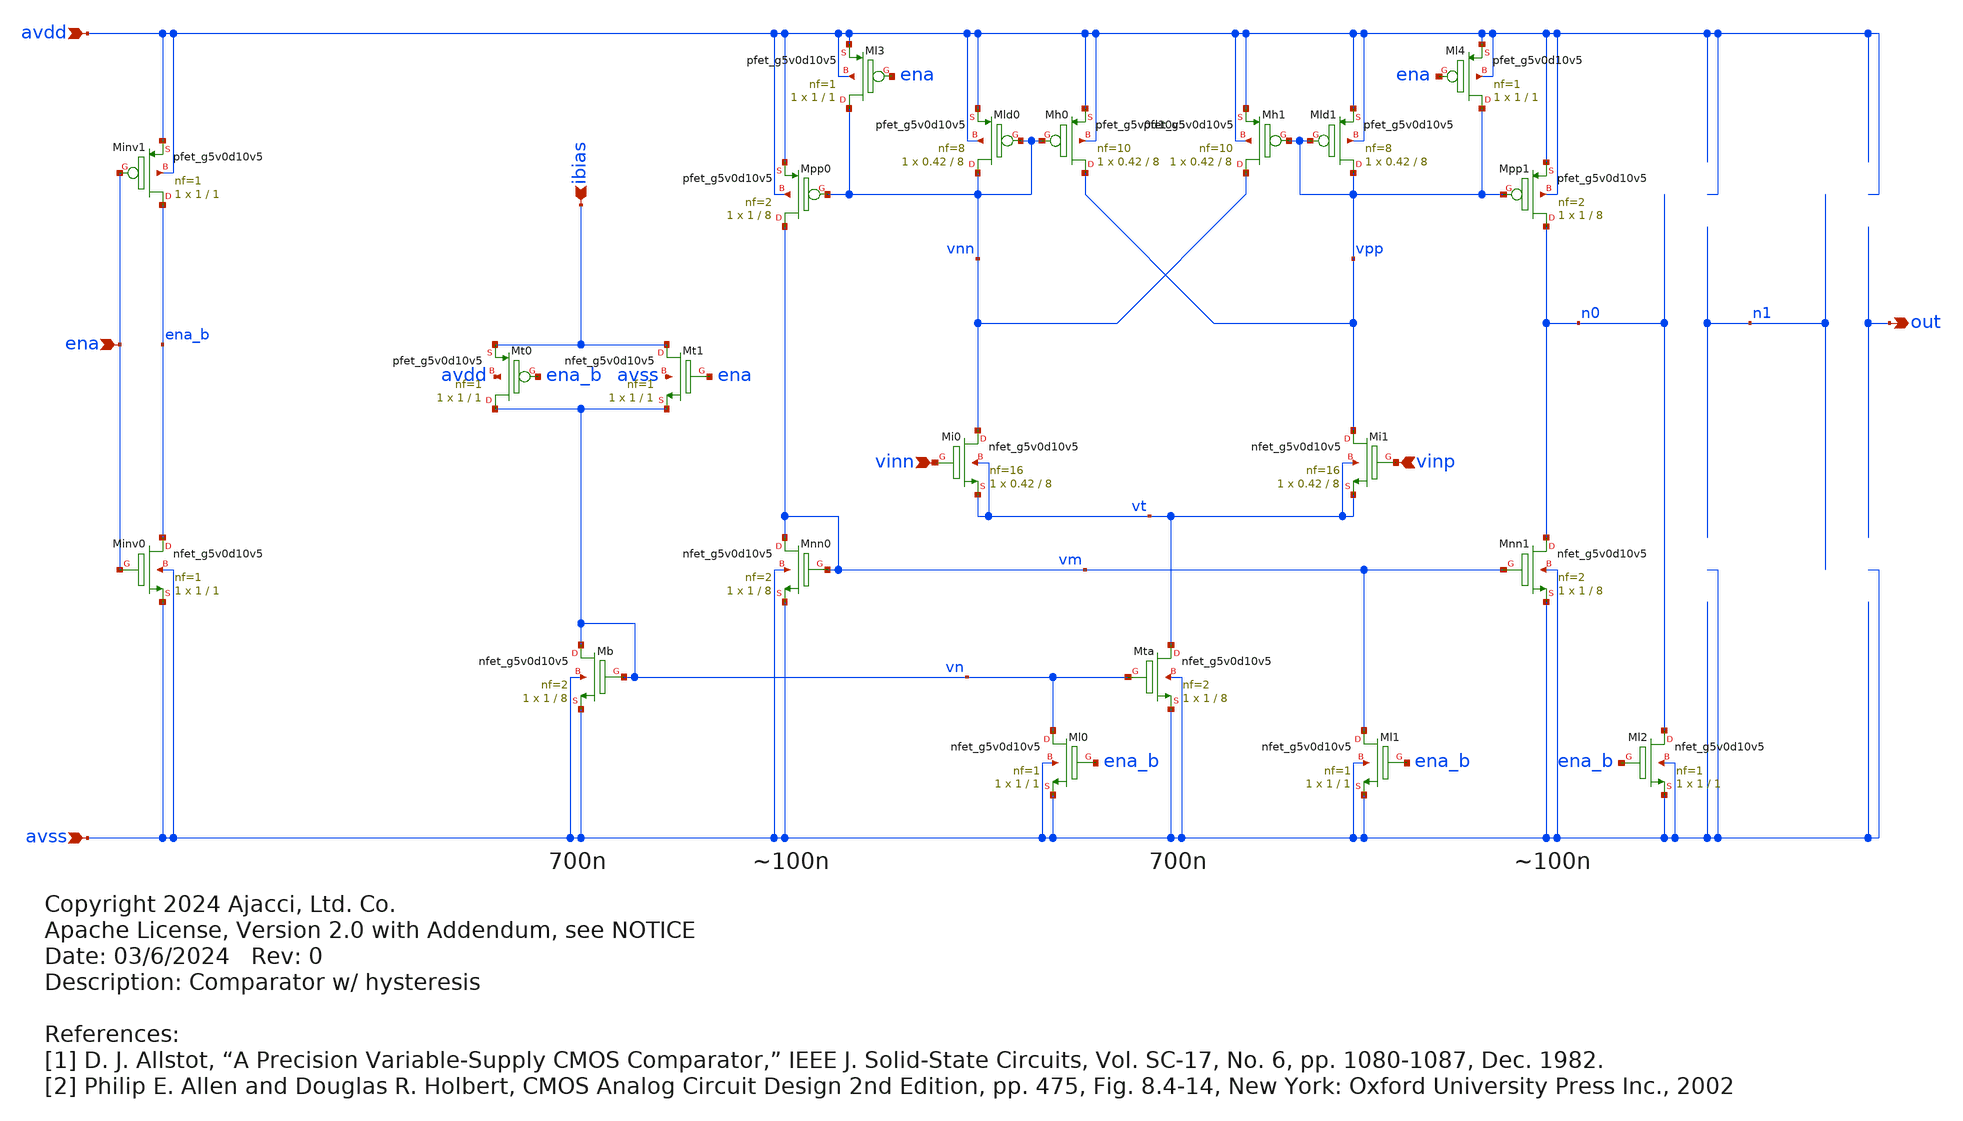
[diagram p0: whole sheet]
** sch_path: xschem/comparator_wip.sch
* Copyright 2024 Ajacci, Ltd. Co.
* Apache License, Version 2.0 with Addendum, see NOTICE
**.subckt comparator_wip ena avdd avss ibias vinn vinp out
*.ipin ena
*.ipin avdd
*.ipin avss
*.ipin ibias
*.ipin vinn
*.ipin vinp
*.opin out
XMi0 vnn vinn vt vt sky130_fd_pr__nfet_g5v0d10v5 L=8 W=0.42 nf=16 ad='int((nf+1)/2) * W/nf * 0.29' as='int((nf+2)/2) * W/nf * 0.29'
+ pd='2*int((nf+1)/2) * (W/nf + 0.29)' ps='2*int((nf+2)/2) * (W/nf + 0.29)' nrd='0.29 / W' nrs='0.29 / W'
+ sa=0 sb=0 sd=0 mult=1 m=1
XMi1 vpp vinp vt vt sky130_fd_pr__nfet_g5v0d10v5 L=8 W=0.42 nf=16 ad='int((nf+1)/2) * W/nf * 0.29' as='int((nf+2)/2) * W/nf * 0.29'
+ pd='2*int((nf+1)/2) * (W/nf + 0.29)' ps='2*int((nf+2)/2) * (W/nf + 0.29)' nrd='0.29 / W' nrs='0.29 / W'
+ sa=0 sb=0 sd=0 mult=1 m=1
XMb vn vn avss avss sky130_fd_pr__nfet_g5v0d10v5 L=8 W=1 nf=2 ad='int((nf+1)/2) * W/nf * 0.29' as='int((nf+2)/2) * W/nf * 0.29'
+ pd='2*int((nf+1)/2) * (W/nf + 0.29)' ps='2*int((nf+2)/2) * (W/nf + 0.29)' nrd='0.29 / W' nrs='0.29 / W'
+ sa=0 sb=0 sd=0 mult=1 m=1
XMta vt vn avss avss sky130_fd_pr__nfet_g5v0d10v5 L=8 W=1 nf=2 ad='int((nf+1)/2) * W/nf * 0.29' as='int((nf+2)/2) * W/nf * 0.29'
+ pd='2*int((nf+1)/2) * (W/nf + 0.29)' ps='2*int((nf+2)/2) * (W/nf + 0.29)' nrd='0.29 / W' nrs='0.29 / W'
+ sa=0 sb=0 sd=0 mult=1 m=1
XMld1 vpp vpp avdd avdd sky130_fd_pr__pfet_g5v0d10v5 L=8 W=0.42 nf=8 ad='int((nf+1)/2) * W/nf * 0.29'
+ as='int((nf+2)/2) * W/nf * 0.29' pd='2*int((nf+1)/2) * (W/nf + 0.29)' ps='2*int((nf+2)/2) * (W/nf + 0.29)'
+ nrd='0.29 / W' nrs='0.29 / W' sa=0 sb=0 sd=0 mult=1 m=1
XMh1 vnn vpp avdd avdd sky130_fd_pr__pfet_g5v0d10v5 L=8 W=0.42 nf=10 ad='int((nf+1)/2) * W/nf * 0.29'
+ as='int((nf+2)/2) * W/nf * 0.29' pd='2*int((nf+1)/2) * (W/nf + 0.29)' ps='2*int((nf+2)/2) * (W/nf + 0.29)'
+ nrd='0.29 / W' nrs='0.29 / W' sa=0 sb=0 sd=0 mult=1 m=1
XMh0 vpp vnn avdd avdd sky130_fd_pr__pfet_g5v0d10v5 L=8 W=0.42 nf=10 ad='int((nf+1)/2) * W/nf * 0.29'
+ as='int((nf+2)/2) * W/nf * 0.29' pd='2*int((nf+1)/2) * (W/nf + 0.29)' ps='2*int((nf+2)/2) * (W/nf + 0.29)'
+ nrd='0.29 / W' nrs='0.29 / W' sa=0 sb=0 sd=0 mult=1 m=1
XMld0 vnn vnn avdd avdd sky130_fd_pr__pfet_g5v0d10v5 L=8 W=0.42 nf=8 ad='int((nf+1)/2) * W/nf * 0.29'
+ as='int((nf+2)/2) * W/nf * 0.29' pd='2*int((nf+1)/2) * (W/nf + 0.29)' ps='2*int((nf+2)/2) * (W/nf + 0.29)'
+ nrd='0.29 / W' nrs='0.29 / W' sa=0 sb=0 sd=0 mult=1 m=1
XMnn1 n0 vm avss avss sky130_fd_pr__nfet_g5v0d10v5 L=8 W=1 nf=2 ad='int((nf+1)/2) * W/nf * 0.29' as='int((nf+2)/2) * W/nf * 0.29'
+ pd='2*int((nf+1)/2) * (W/nf + 0.29)' ps='2*int((nf+2)/2) * (W/nf + 0.29)' nrd='0.29 / W' nrs='0.29 / W'
+ sa=0 sb=0 sd=0 mult=1 m=1
XMnn0 vm vm avss avss sky130_fd_pr__nfet_g5v0d10v5 L=8 W=1 nf=2 ad='int((nf+1)/2) * W/nf * 0.29' as='int((nf+2)/2) * W/nf * 0.29'
+ pd='2*int((nf+1)/2) * (W/nf + 0.29)' ps='2*int((nf+2)/2) * (W/nf + 0.29)' nrd='0.29 / W' nrs='0.29 / W'
+ sa=0 sb=0 sd=0 mult=1 m=1
XMpp1 n0 vpp avdd avdd sky130_fd_pr__pfet_g5v0d10v5 L=8 W=1 nf=2 ad='int((nf+1)/2) * W/nf * 0.29' as='int((nf+2)/2) * W/nf * 0.29'
+ pd='2*int((nf+1)/2) * (W/nf + 0.29)' ps='2*int((nf+2)/2) * (W/nf + 0.29)' nrd='0.29 / W' nrs='0.29 / W'
+ sa=0 sb=0 sd=0 mult=1 m=1
XMpp0 vm vnn avdd avdd sky130_fd_pr__pfet_g5v0d10v5 L=8 W=1 nf=2 ad='int((nf+1)/2) * W/nf * 0.29' as='int((nf+2)/2) * W/nf * 0.29'
+ pd='2*int((nf+1)/2) * (W/nf + 0.29)' ps='2*int((nf+2)/2) * (W/nf + 0.29)' nrd='0.29 / W' nrs='0.29 / W'
+ sa=0 sb=0 sd=0 mult=1 m=1
XMt1 ibias ena vn avss sky130_fd_pr__nfet_g5v0d10v5 L=1 W=1 nf=1 ad='int((nf+1)/2) * W/nf * 0.29' as='int((nf+2)/2) * W/nf * 0.29'
+ pd='2*int((nf+1)/2) * (W/nf + 0.29)' ps='2*int((nf+2)/2) * (W/nf + 0.29)' nrd='0.29 / W' nrs='0.29 / W'
+ sa=0 sb=0 sd=0 mult=1 m=1
XMt0 vn ena_b ibias avdd sky130_fd_pr__pfet_g5v0d10v5 L=1 W=1 nf=1 ad='int((nf+1)/2) * W/nf * 0.29' as='int((nf+2)/2) * W/nf * 0.29'
+ pd='2*int((nf+1)/2) * (W/nf + 0.29)' ps='2*int((nf+2)/2) * (W/nf + 0.29)' nrd='0.29 / W' nrs='0.29 / W'
+ sa=0 sb=0 sd=0 mult=1 m=1
XMinv0 ena_b ena avss avss sky130_fd_pr__nfet_g5v0d10v5 L=1 W=1 nf=1 ad='int((nf+1)/2) * W/nf * 0.29'
+ as='int((nf+2)/2) * W/nf * 0.29' pd='2*int((nf+1)/2) * (W/nf + 0.29)' ps='2*int((nf+2)/2) * (W/nf + 0.29)'
+ nrd='0.29 / W' nrs='0.29 / W' sa=0 sb=0 sd=0 mult=1 m=1
XMinv1 ena_b ena avdd avdd sky130_fd_pr__pfet_g5v0d10v5 L=1 W=1 nf=1 ad='int((nf+1)/2) * W/nf * 0.29'
+ as='int((nf+2)/2) * W/nf * 0.29' pd='2*int((nf+1)/2) * (W/nf + 0.29)' ps='2*int((nf+2)/2) * (W/nf + 0.29)'
+ nrd='0.29 / W' nrs='0.29 / W' sa=0 sb=0 sd=0 mult=1 m=1
XMl0 vn ena_b avss avss sky130_fd_pr__nfet_g5v0d10v5 L=1 W=1 nf=1 ad='int((nf+1)/2) * W/nf * 0.29' as='int((nf+2)/2) * W/nf * 0.29'
+ pd='2*int((nf+1)/2) * (W/nf + 0.29)' ps='2*int((nf+2)/2) * (W/nf + 0.29)' nrd='0.29 / W' nrs='0.29 / W'
+ sa=0 sb=0 sd=0 mult=1 m=1
XMl1 vm ena_b avss avss sky130_fd_pr__nfet_g5v0d10v5 L=1 W=1 nf=1 ad='int((nf+1)/2) * W/nf * 0.29' as='int((nf+2)/2) * W/nf * 0.29'
+ pd='2*int((nf+1)/2) * (W/nf + 0.29)' ps='2*int((nf+2)/2) * (W/nf + 0.29)' nrd='0.29 / W' nrs='0.29 / W'
+ sa=0 sb=0 sd=0 mult=1 m=1
XMl3 vnn ena avdd avdd sky130_fd_pr__pfet_g5v0d10v5 L=1 W=1 nf=1 ad='int((nf+1)/2) * W/nf * 0.29' as='int((nf+2)/2) * W/nf * 0.29'
+ pd='2*int((nf+1)/2) * (W/nf + 0.29)' ps='2*int((nf+2)/2) * (W/nf + 0.29)' nrd='0.29 / W' nrs='0.29 / W'
+ sa=0 sb=0 sd=0 mult=1 m=1
XMl4 vpp ena avdd avdd sky130_fd_pr__pfet_g5v0d10v5 L=1 W=1 nf=1 ad='int((nf+1)/2) * W/nf * 0.29' as='int((nf+2)/2) * W/nf * 0.29'
+ pd='2*int((nf+1)/2) * (W/nf + 0.29)' ps='2*int((nf+2)/2) * (W/nf + 0.29)' nrd='0.29 / W' nrs='0.29 / W'
+ sa=0 sb=0 sd=0 mult=1 m=1
XMl2 n0 ena_b avss avss sky130_fd_pr__nfet_g5v0d10v5 L=1 W=1 nf=1 ad='int((nf+1)/2) * W/nf * 0.29' as='int((nf+2)/2) * W/nf * 0.29'
+ pd='2*int((nf+1)/2) * (W/nf + 0.29)' ps='2*int((nf+2)/2) * (W/nf + 0.29)' nrd='0.29 / W' nrs='0.29 / W'
+ sa=0 sb=0 sd=0 mult=1 m=1
**.ends
.end
